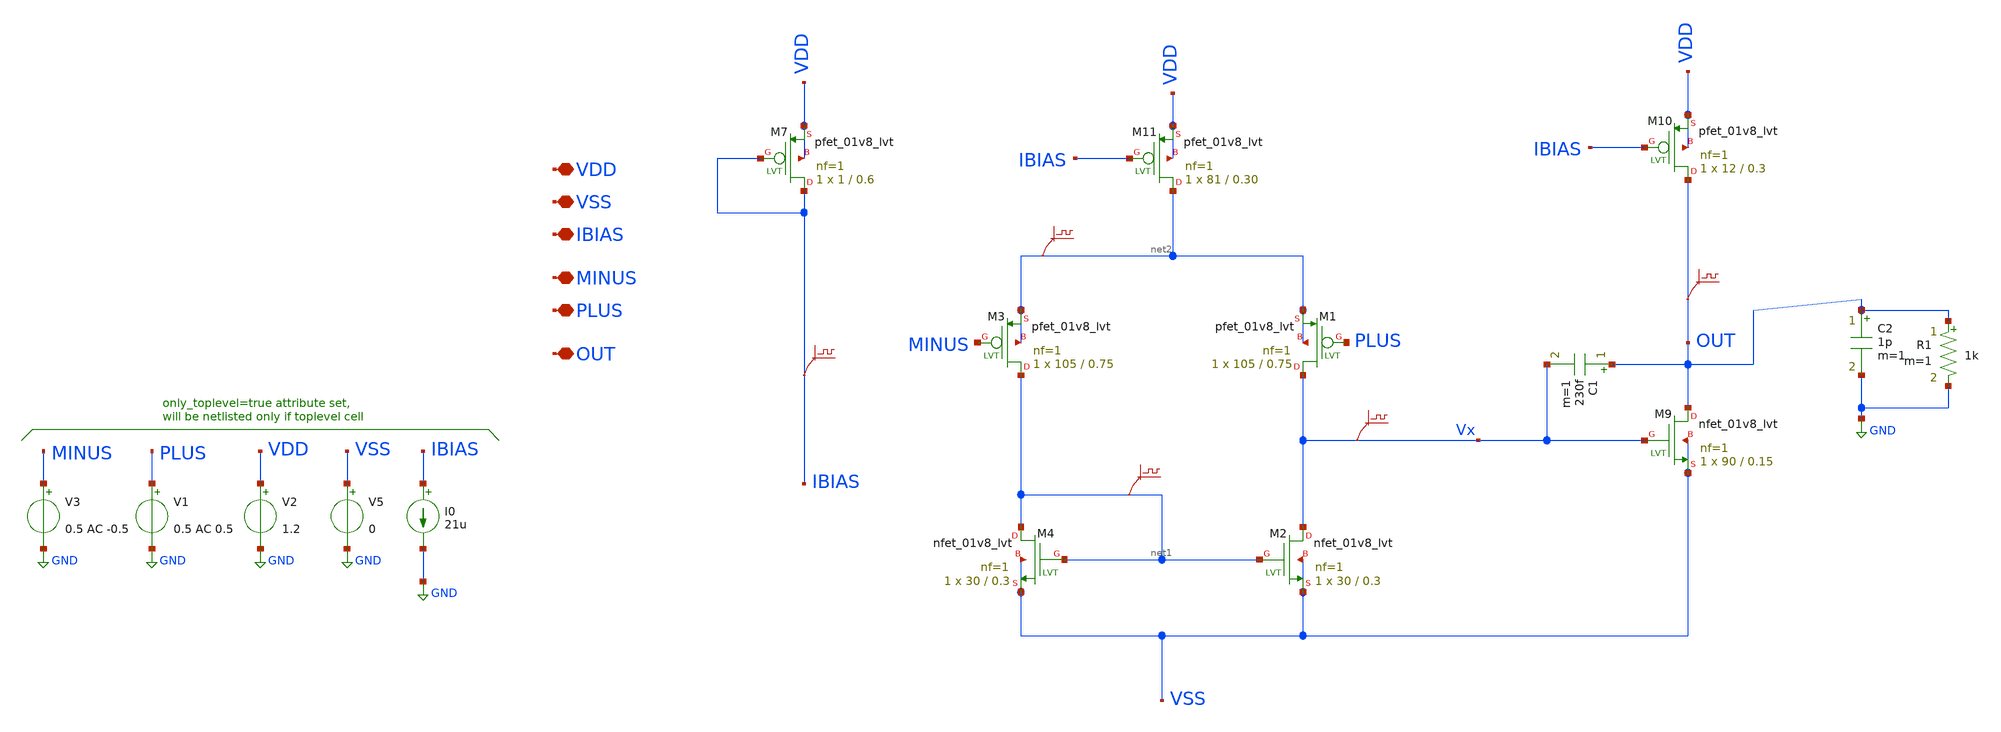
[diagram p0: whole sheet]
** sch_path: untitled-1.sch
**.subckt untitled-1 VDD VSS MINUS PLUS OUT IBIAS
*.iopin VDD
*.iopin VSS
*.iopin MINUS
*.iopin PLUS
*.iopin OUT
*.iopin IBIAS
V1 PLUS GND 0.5 AC 0.5
V3 MINUS GND 0.5 AC -0.5
V5 VSS GND 0
I0 IBIAS GND 21u
V2 VDD GND 1.2
.save v(vx)
XM4 net1 net1 VSS VSS sky130_fd_pr__nfet_01v8_lvt L=0.3 W=30 nf=1 ad='int((nf+1)/2) * W/nf * 0.29' as='int((nf+2)/2) * W/nf * 0.29'
+ pd='2*int((nf+1)/2) * (W/nf + 0.29)' ps='2*int((nf+2)/2) * (W/nf + 0.29)' nrd='0.29 / W' nrs='0.29 / W'
+ sa=0 sb=0 sd=0 mult=1 m=1
XM2 Vx net1 VSS VSS sky130_fd_pr__nfet_01v8_lvt L=0.3 W=30 nf=1 ad='int((nf+1)/2) * W/nf * 0.29' as='int((nf+2)/2) * W/nf * 0.29'
+ pd='2*int((nf+1)/2) * (W/nf + 0.29)' ps='2*int((nf+2)/2) * (W/nf + 0.29)' nrd='0.29 / W' nrs='0.29 / W'
+ sa=0 sb=0 sd=0 mult=1 m=1
XM3 net1 MINUS net2 net2 sky130_fd_pr__pfet_01v8_lvt L=0.75 W=105 nf=1 ad='int((nf+1)/2) * W/nf * 0.29'
+ as='int((nf+2)/2) * W/nf * 0.29' pd='2*int((nf+1)/2) * (W/nf + 0.29)' ps='2*int((nf+2)/2) * (W/nf + 0.29)'
+ nrd='0.29 / W' nrs='0.29 / W' sa=0 sb=0 sd=0 mult=1 m=1
XM1 Vx PLUS net2 net2 sky130_fd_pr__pfet_01v8_lvt L=0.75 W=105 nf=1 ad='int((nf+1)/2) * W/nf * 0.29'
+ as='int((nf+2)/2) * W/nf * 0.29' pd='2*int((nf+1)/2) * (W/nf + 0.29)' ps='2*int((nf+2)/2) * (W/nf + 0.29)'
+ nrd='0.29 / W' nrs='0.29 / W' sa=0 sb=0 sd=0 mult=1 m=1
XM7 IBIAS IBIAS VDD VDD sky130_fd_pr__pfet_01v8_lvt L=0.6 W=1 nf=1 ad='int((nf+1)/2) * W/nf * 0.29' as='int((nf+2)/2) * W/nf * 0.29'
+ pd='2*int((nf+1)/2) * (W/nf + 0.29)' ps='2*int((nf+2)/2) * (W/nf + 0.29)' nrd='0.29 / W' nrs='0.29 / W'
+ sa=0 sb=0 sd=0 mult=1 m=1
.save v(net2)
XM9 OUT Vx VSS VSS sky130_fd_pr__nfet_01v8_lvt L=0.15 W=90 nf=1 ad='int((nf+1)/2) * W/nf * 0.29' as='int((nf+2)/2) * W/nf * 0.29'
+ pd='2*int((nf+1)/2) * (W/nf + 0.29)' ps='2*int((nf+2)/2) * (W/nf + 0.29)' nrd='0.29 / W' nrs='0.29 / W'
+ sa=0 sb=0 sd=0 mult=1 m=1
XM10 OUT IBIAS VDD VDD sky130_fd_pr__pfet_01v8_lvt L=0.3 W=12 nf=1 ad='int((nf+1)/2) * W/nf * 0.29' as='int((nf+2)/2) * W/nf * 0.29'
+ pd='2*int((nf+1)/2) * (W/nf + 0.29)' ps='2*int((nf+2)/2) * (W/nf + 0.29)' nrd='0.29 / W' nrs='0.29 / W'
+ sa=0 sb=0 sd=0 mult=1 m=1
XM11 net2 IBIAS VDD VDD sky130_fd_pr__pfet_01v8_lvt L=0.30 W=81 nf=1 ad='int((nf+1)/2) * W/nf * 0.29'
+ as='int((nf+2)/2) * W/nf * 0.29' pd='2*int((nf+1)/2) * (W/nf + 0.29)' ps='2*int((nf+2)/2) * (W/nf + 0.29)'
+ nrd='0.29 / W' nrs='0.29 / W' sa=0 sb=0 sd=0 mult=1 m=1
.save v(net1)
.save v(out)
.save v(ibias)
C1 OUT Vx 230f m=1
C2 OUT GND 1p m=1
R1 OUT GND 1k m=1
**** begin user architecture code

** opencircuitdesign pdks install
.lib $::SKYWATER_MODELS/sky130.lib.spice tt





.control

*ac dec 20 1 10g
*run
*plot db(v(out)) 180*cph(v(out))/pi
*plot db(v(Vx)) 180*cph(v(Vx))/pi
*reset


save @m.xm5.msky130_fd_pr__nfet_01v8_lvt[gm]
save @m.xm5.msky130_fd_pr__nfet_01v8_lvt[vth]
save @m.xm5.msky130_fd_pr__nfet_01v8_lvt[vdsat]
save @m.xm5.msky130_fd_pr__nfet_01v8_lvt[vds]
save @m.xm5.msky130_fd_pr__nfet_01v8_lvt[id]
save @m.xm5.msky130_fd_pr__nfet_01v8_lvt[gds]

save @m.xm6.msky130_fd_pr__pfet_01v8_lvt[gm]
save @m.xm6.msky130_fd_pr__pfet_01v8_lvt[vth]
save @m.xm6.msky130_fd_pr__pfet_01v8_lvt[vdsat]
save @m.xm6.msky130_fd_pr__pfet_01v8_lvt[vds]
save @m.xm6.msky130_fd_pr__pfet_01v8_lvt[id]
save @m.xm6.msky130_fd_pr__pfet_01v8_lvt[gds]

save @m.xm9.msky130_fd_pr__nfet_01v8_lvt[gm]
save @m.xm9.msky130_fd_pr__nfet_01v8_lvt[vth]
save @m.xm9.msky130_fd_pr__nfet_01v8_lvt[vdsat]
save @m.xm9.msky130_fd_pr__nfet_01v8_lvt[vds]
save @m.xm9.msky130_fd_pr__nfet_01v8_lvt[id]
save @m.xm9.msky130_fd_pr__nfet_01v8_lvt[gds]

save @m.xm10.msky130_fd_pr__pfet_01v8_lvt[gm]
save @m.xm10.msky130_fd_pr__pfet_01v8_lvt[vth]
save @m.xm10.msky130_fd_pr__pfet_01v8_lvt[vdsat]
save @m.xm10.msky130_fd_pr__pfet_01v8_lvt[vds]
save @m.xm10.msky130_fd_pr__pfet_01v8_lvt[id]
save @m.xm10.msky130_fd_pr__pfet_01v8_lvt[gds]

save @m.xm11.msky130_fd_pr__pfet_01v8_lvt[gm]
save @m.xm11.msky130_fd_pr__pfet_01v8_lvt[vth]
save @m.xm11.msky130_fd_pr__pfet_01v8_lvt[vdsat]
save @m.xm11.msky130_fd_pr__pfet_01v8_lvt[vds]
save @m.xm11.msky130_fd_pr__pfet_01v8_lvt[id]
save @m.xm11.msky130_fd_pr__pfet_01v8_lvt[gds]


save all
op

write untitled-1.raw

.endc


**** end user architecture code
**.ends
.GLOBAL GND
.end
